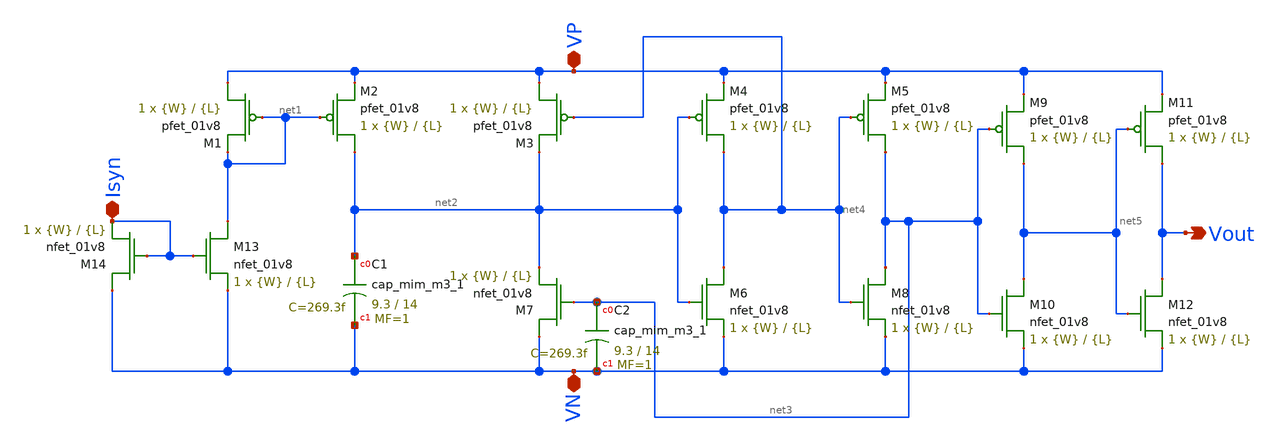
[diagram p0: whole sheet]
** sch_path: schematic/besrour_neuron_cm.sch
**.subckt besrour_neuron_cm VP VN Isyn Vout
*.iopin VP
*.iopin VN
*.iopin Isyn
*.opin Vout
XM2 net2 net1 VP VDD sky130_fd_pr__pfet_01v8 L={L} W={W} nf=1 ad='int((nf+1)/2) * W/nf * 0.29' as='int((nf+2)/2) * W/nf * 0.29'
+ pd='2*int((nf+1)/2) * (W/nf + 0.29)' ps='2*int((nf+2)/2) * (W/nf + 0.29)' nrd='0.29 / W' nrs='0.29 / W'
+ sa=0 sb=0 sd=0 mult=1 m=1
XM3 VP net4 net2 VDD sky130_fd_pr__pfet_01v8 L={L} W={W} nf=1 ad='int((nf+1)/2) * W/nf * 0.29' as='int((nf+2)/2) * W/nf * 0.29'
+ pd='2*int((nf+1)/2) * (W/nf + 0.29)' ps='2*int((nf+2)/2) * (W/nf + 0.29)' nrd='0.29 / W' nrs='0.29 / W'
+ sa=0 sb=0 sd=0 mult=1 m=1
XM4 net4 net2 VP VDD sky130_fd_pr__pfet_01v8 L={L} W={W} nf=1 ad='int((nf+1)/2) * W/nf * 0.29' as='int((nf+2)/2) * W/nf * 0.29'
+ pd='2*int((nf+1)/2) * (W/nf + 0.29)' ps='2*int((nf+2)/2) * (W/nf + 0.29)' nrd='0.29 / W' nrs='0.29 / W'
+ sa=0 sb=0 sd=0 mult=1 m=1
XM5 net3 net4 VP VDD sky130_fd_pr__pfet_01v8 L={L} W={W} nf=1 ad='int((nf+1)/2) * W/nf * 0.29' as='int((nf+2)/2) * W/nf * 0.29'
+ pd='2*int((nf+1)/2) * (W/nf + 0.29)' ps='2*int((nf+2)/2) * (W/nf + 0.29)' nrd='0.29 / W' nrs='0.29 / W'
+ sa=0 sb=0 sd=0 mult=1 m=1
XM6 net4 net2 VN GND sky130_fd_pr__nfet_01v8 L={L} W={W} nf=1 ad='int((nf+1)/2) * W/nf * 0.29' as='int((nf+2)/2) * W/nf * 0.29'
+ pd='2*int((nf+1)/2) * (W/nf + 0.29)' ps='2*int((nf+2)/2) * (W/nf + 0.29)' nrd='0.29 / W' nrs='0.29 / W'
+ sa=0 sb=0 sd=0 mult=1 m=1
XM8 net3 net4 VN GND sky130_fd_pr__nfet_01v8 L={L} W={W} nf=1 ad='int((nf+1)/2) * W/nf * 0.29' as='int((nf+2)/2) * W/nf * 0.29'
+ pd='2*int((nf+1)/2) * (W/nf + 0.29)' ps='2*int((nf+2)/2) * (W/nf + 0.29)' nrd='0.29 / W' nrs='0.29 / W'
+ sa=0 sb=0 sd=0 mult=1 m=1
XM9 net5 net3 VP VDD sky130_fd_pr__pfet_01v8 L={L} W={W} nf=1 ad='int((nf+1)/2) * W/nf * 0.29' as='int((nf+2)/2) * W/nf * 0.29'
+ pd='2*int((nf+1)/2) * (W/nf + 0.29)' ps='2*int((nf+2)/2) * (W/nf + 0.29)' nrd='0.29 / W' nrs='0.29 / W'
+ sa=0 sb=0 sd=0 mult=1 m=1
XM10 net5 net3 VN GND sky130_fd_pr__nfet_01v8 L={L} W={W} nf=1 ad='int((nf+1)/2) * W/nf * 0.29' as='int((nf+2)/2) * W/nf * 0.29'
+ pd='2*int((nf+1)/2) * (W/nf + 0.29)' ps='2*int((nf+2)/2) * (W/nf + 0.29)' nrd='0.29 / W' nrs='0.29 / W'
+ sa=0 sb=0 sd=0 mult=1 m=1
XM11 Vout net5 VP VDD sky130_fd_pr__pfet_01v8 L={L} W={W} nf=1 ad='int((nf+1)/2) * W/nf * 0.29' as='int((nf+2)/2) * W/nf * 0.29'
+ pd='2*int((nf+1)/2) * (W/nf + 0.29)' ps='2*int((nf+2)/2) * (W/nf + 0.29)' nrd='0.29 / W' nrs='0.29 / W'
+ sa=0 sb=0 sd=0 mult=1 m=1
XM12 Vout net5 VN GND sky130_fd_pr__nfet_01v8 L={L} W={W} nf=1 ad='int((nf+1)/2) * W/nf * 0.29' as='int((nf+2)/2) * W/nf * 0.29'
+ pd='2*int((nf+1)/2) * (W/nf + 0.29)' ps='2*int((nf+2)/2) * (W/nf + 0.29)' nrd='0.29 / W' nrs='0.29 / W'
+ sa=0 sb=0 sd=0 mult=1 m=1
XM13 net1 Isyn VN GND sky130_fd_pr__nfet_01v8 L={L} W={W} nf=1 ad='int((nf+1)/2) * W/nf * 0.29' as='int((nf+2)/2) * W/nf * 0.29'
+ pd='2*int((nf+1)/2) * (W/nf + 0.29)' ps='2*int((nf+2)/2) * (W/nf + 0.29)' nrd='0.29 / W' nrs='0.29 / W'
+ sa=0 sb=0 sd=0 mult=1 m=1
XM14 VN Isyn Isyn GND sky130_fd_pr__nfet_01v8 L={L} W={W} nf=1 ad='int((nf+1)/2) * W/nf * 0.29' as='int((nf+2)/2) * W/nf * 0.29'
+ pd='2*int((nf+1)/2) * (W/nf + 0.29)' ps='2*int((nf+2)/2) * (W/nf + 0.29)' nrd='0.29 / W' nrs='0.29 / W'
+ sa=0 sb=0 sd=0 mult=1 m=1
XM1 VP net1 net1 VDD sky130_fd_pr__pfet_01v8 L={L} W={W} nf=1 ad='int((nf+1)/2) * W/nf * 0.29' as='int((nf+2)/2) * W/nf * 0.29'
+ pd='2*int((nf+1)/2) * (W/nf + 0.29)' ps='2*int((nf+2)/2) * (W/nf + 0.29)' nrd='0.29 / W' nrs='0.29 / W'
+ sa=0 sb=0 sd=0 mult=1 m=1
XM7 VN net3 net2 GND sky130_fd_pr__nfet_01v8 L={L} W={W} nf=1 ad='int((nf+1)/2) * W/nf * 0.29' as='int((nf+2)/2) * W/nf * 0.29'
+ pd='2*int((nf+1)/2) * (W/nf + 0.29)' ps='2*int((nf+2)/2) * (W/nf + 0.29)' nrd='0.29 / W' nrs='0.29 / W'
+ sa=0 sb=0 sd=0 mult=1 m=1
XC1 net2 VN sky130_fd_pr__cap_mim_m3_1 W=9.3 L=14 MF=1 m=1
XC2 net3 VN sky130_fd_pr__cap_mim_m3_1 W=9.3 L=14 MF=1 m=1
**.ends
.end
